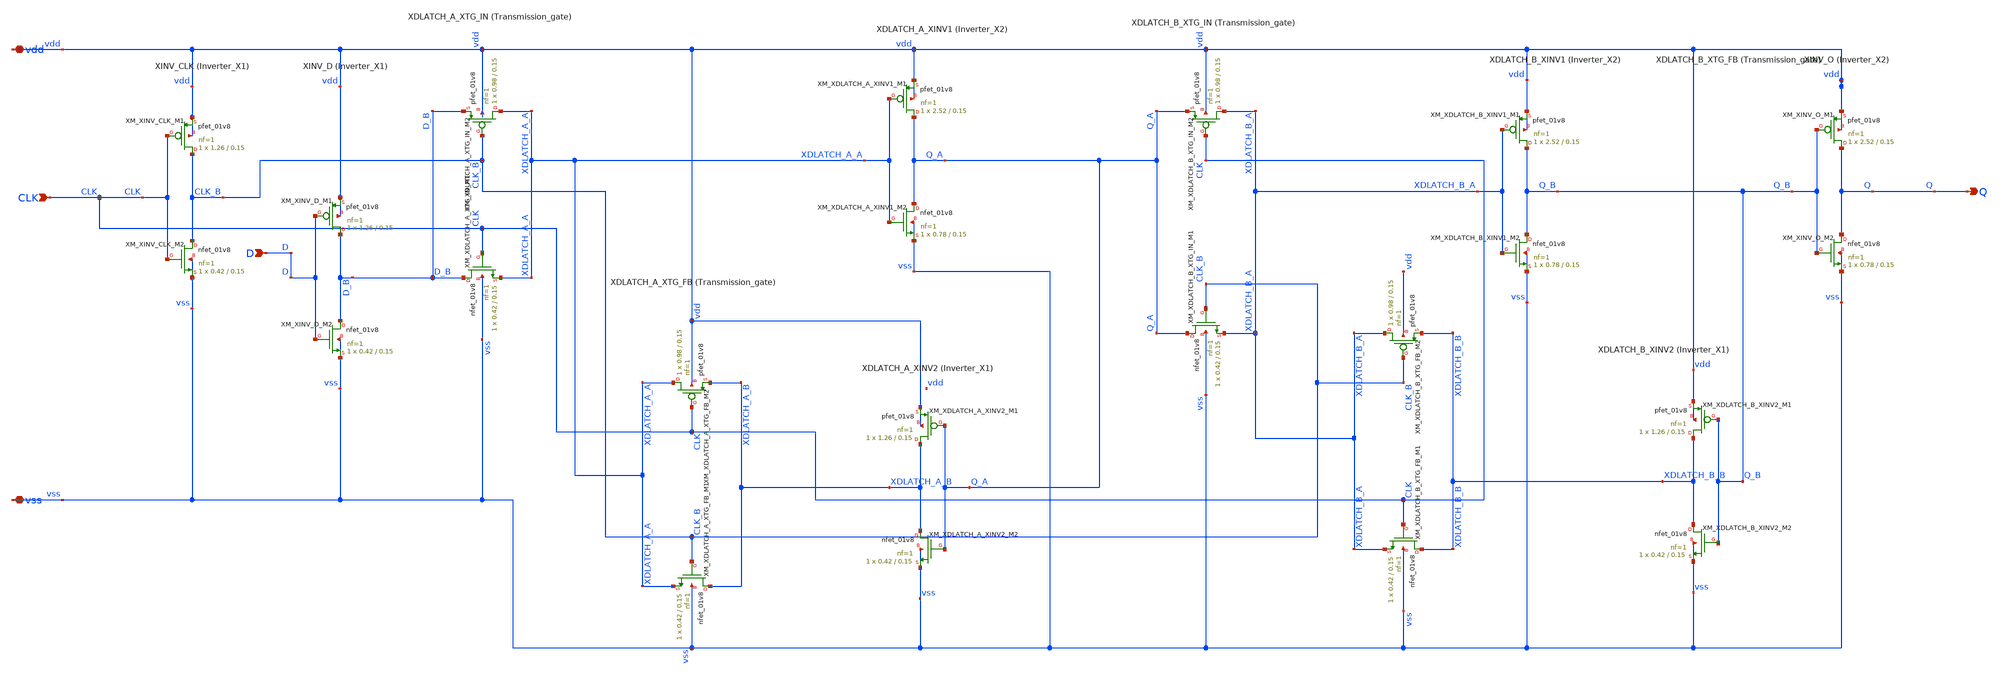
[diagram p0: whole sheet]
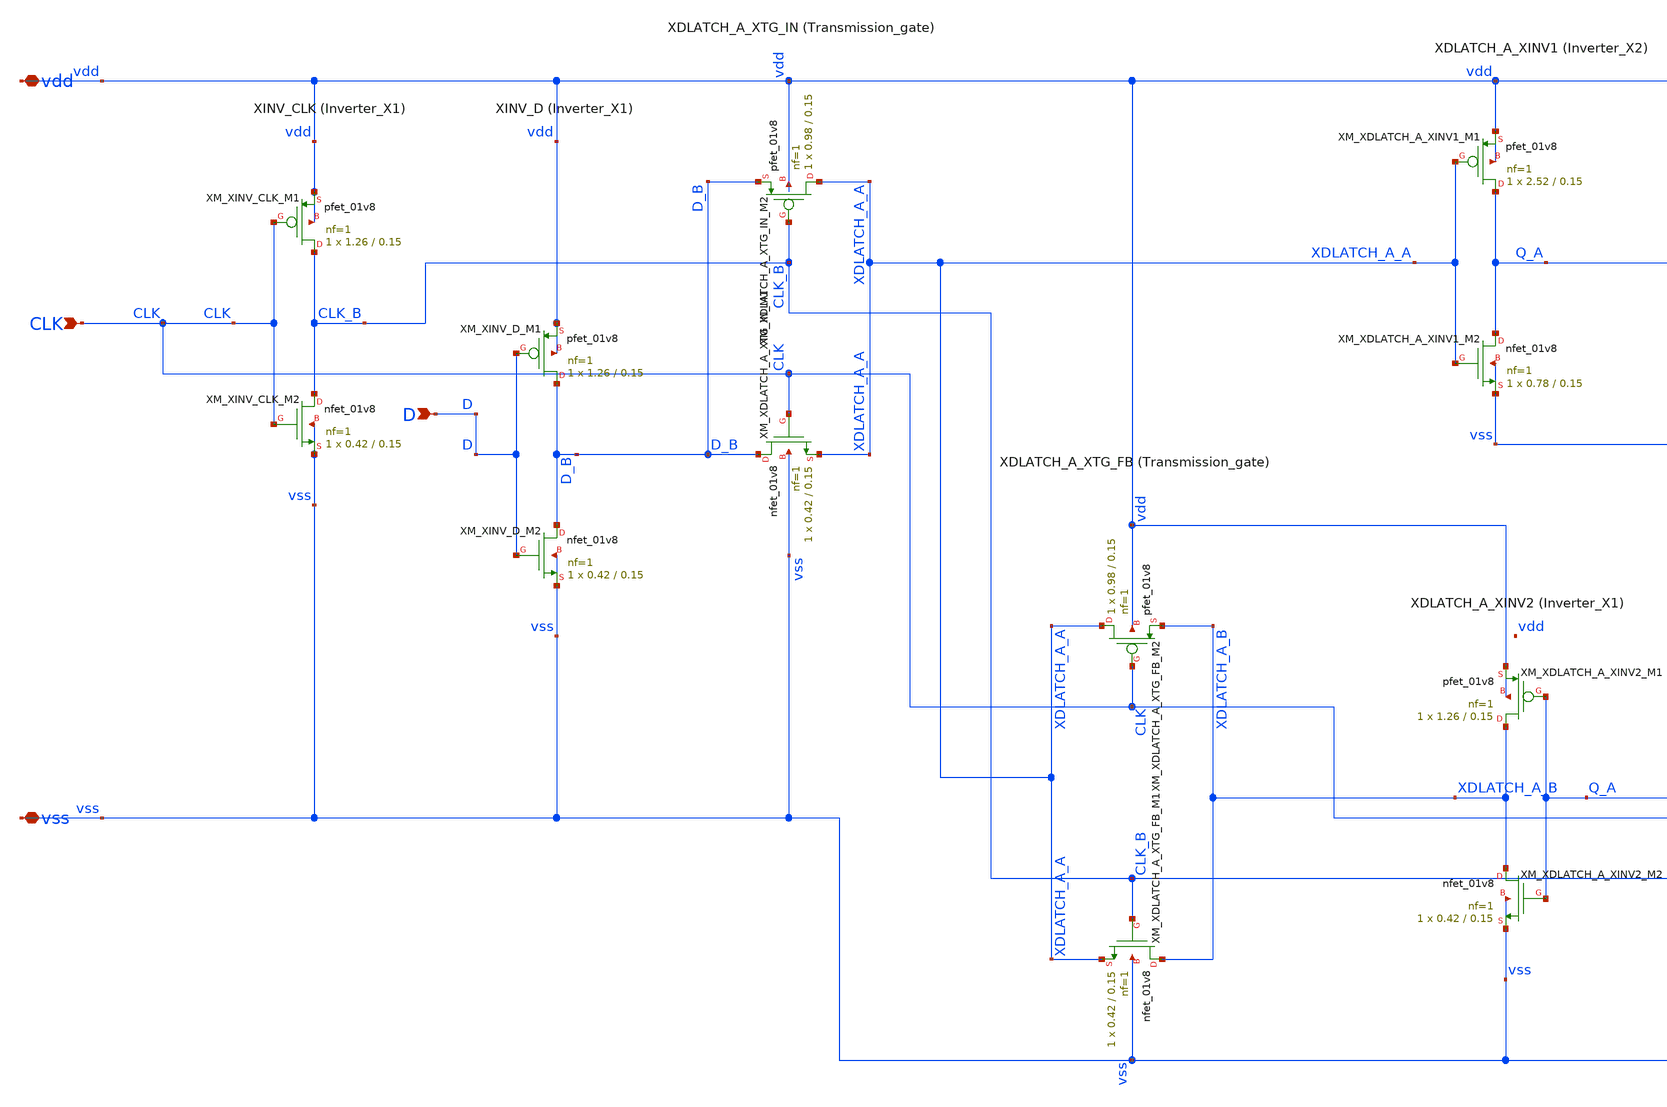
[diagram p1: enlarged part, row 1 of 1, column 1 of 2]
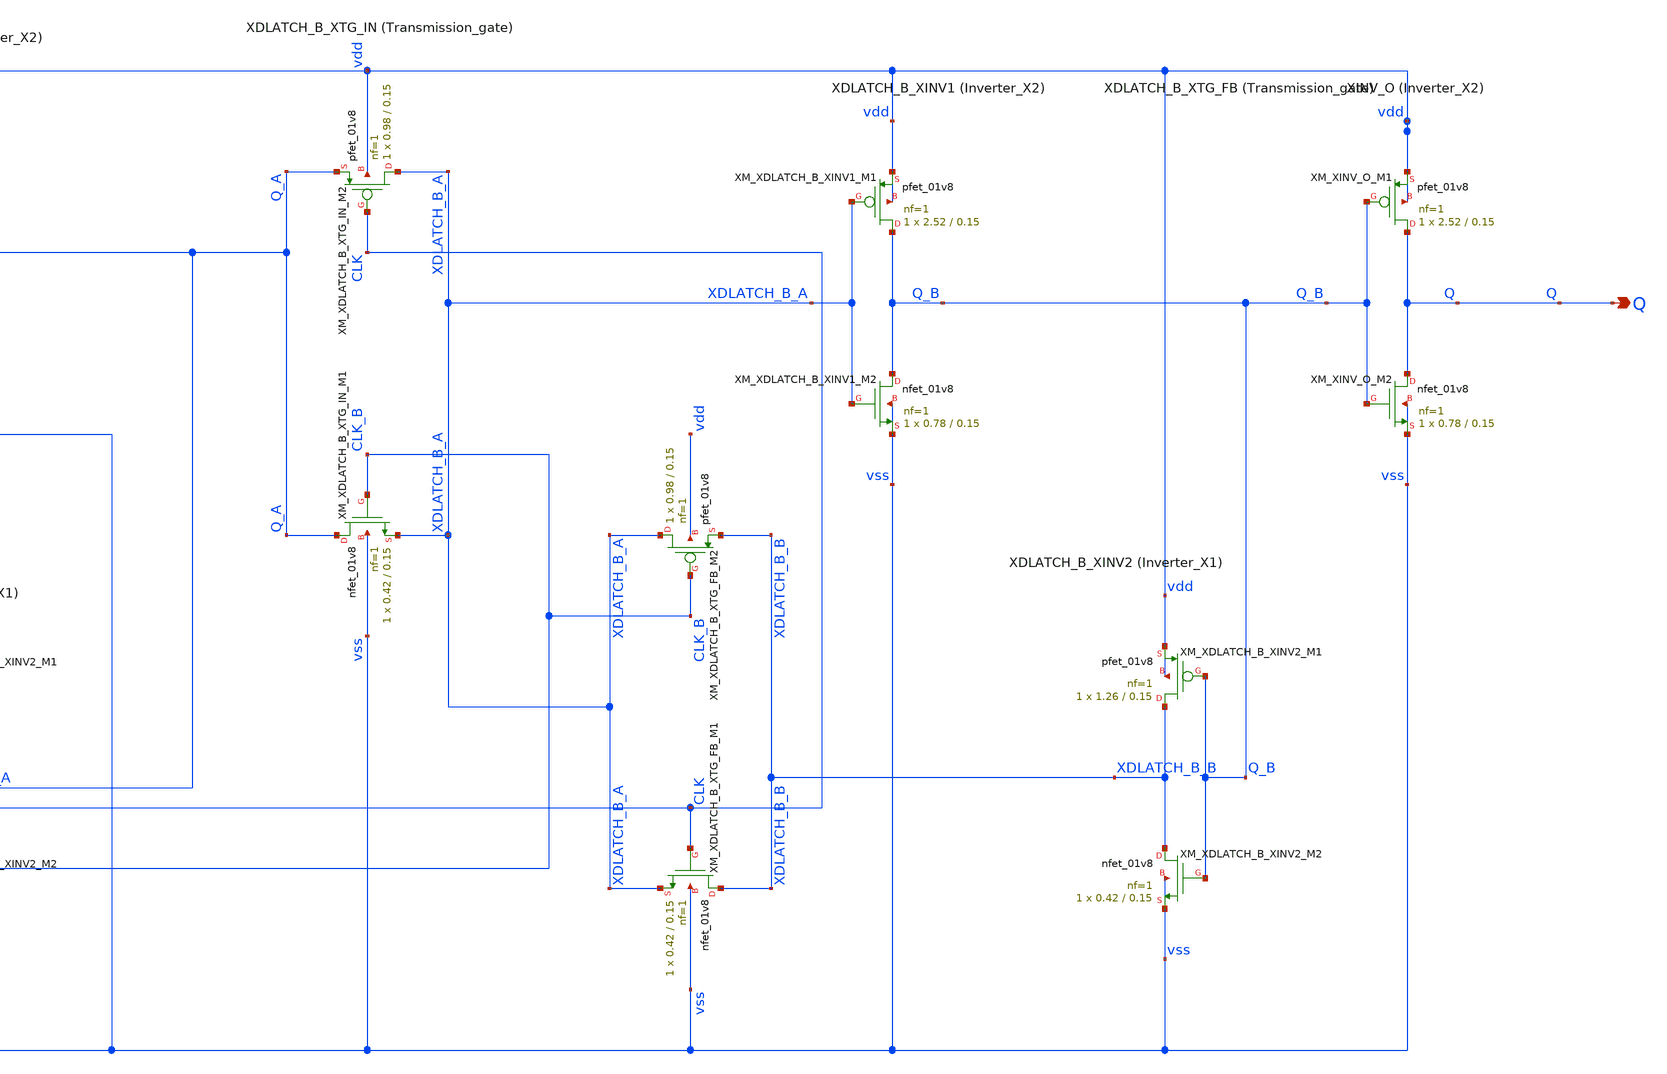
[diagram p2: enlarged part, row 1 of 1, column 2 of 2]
** sch_path: Spice_Netlist/Schematic/dfxtn_flat.sch
**.subckt dfxtn_flat vdd vss D CLK Q
*.iopin vdd
*.iopin vss
*.ipin D
*.ipin CLK
*.opin Q
XXM_XINV_CLK_M1 CLK_B CLK vdd vdd sky130_fd_pr__pfet_01v8 L=0.15 W=1.26 nf=1 ad='int((nf+1)/2) * W/nf * 0.29'
+ as='int((nf+2)/2) * W/nf * 0.29' pd='2*int((nf+1)/2) * (W/nf + 0.29)' ps='2*int((nf+2)/2) * (W/nf + 0.29)'
+ nrd='0.29 / W' nrs='0.29 / W' sa=0 sb=0 sd=0 mult=1 m=1
XXM_XINV_CLK_M2 CLK_B CLK vss vss sky130_fd_pr__nfet_01v8 L=0.15 W=0.42 nf=1 ad='int((1 + 1)/2) * 0.42 / 1 * 0.29'
+ as='int((1 + 2)/2) * 0.42 / 1 * 0.29' pd='2*int((1 + 1)/2) * (0.42 / 1 + 0.29)' ps='2*int((1 + 2)/2) * (0.42 / 1 + 0.29)'
+ nrd='0.29 / 0.42 ' nrs='0.29 / 0.42 ' sa=0 sb=0 sd=0 mult=1 m=1
XXM_XINV_D_M1 D_B D vdd vdd sky130_fd_pr__pfet_01v8 L=0.15 W=1.26 nf=1 ad='int((nf+1)/2) * W/nf * 0.29'
+ as='int((nf+2)/2) * W/nf * 0.29' pd='2*int((nf+1)/2) * (W/nf + 0.29)' ps='2*int((nf+2)/2) * (W/nf + 0.29)'
+ nrd='0.29 / W' nrs='0.29 / W' sa=0 sb=0 sd=0 mult=1 m=1
XXM_XINV_D_M2 D_B D vss vss sky130_fd_pr__nfet_01v8 L=0.15 W=0.42 nf=1 ad='int((1 + 1)/2) * 0.42 / 1 * 0.29'
+ as='int((1 + 2)/2) * 0.42 / 1 * 0.29' pd='2*int((1 + 1)/2) * (0.42 / 1 + 0.29)' ps='2*int((1 + 2)/2) * (0.42 / 1 + 0.29)'
+ nrd='0.29 / 0.42 ' nrs='0.29 / 0.42 ' sa=0 sb=0 sd=0 mult=1 m=1
XXM_XDLATCH_A_XTG_IN_M2 XDLATCH_A_A CLK_B D_B vdd sky130_fd_pr__pfet_01v8 L=0.15 W=0.98 nf=1 ad='int((nf+1)/2) * W/nf * 0.29'
+ as='int((nf+2)/2) * W/nf * 0.29' pd='2*int((nf+1)/2) * (W/nf + 0.29)' ps='2*int((nf+2)/2) * (W/nf + 0.29)'
+ nrd='0.29 / W' nrs='0.29 / W' sa=0 sb=0 sd=0 mult=1 m=1
XXM_XDLATCH_A_XTG_IN_M1 D_B CLK XDLATCH_A_A vss sky130_fd_pr__nfet_01v8 L=0.15 W=0.42 nf=1 ad='int((1 + 1)/2) * 0.42 / 1 * 0.29'
+ as='int((1 + 2)/2) * 0.42 / 1 * 0.29' pd='2*int((1 + 1)/2) * (0.42 / 1 + 0.29)' ps='2*int((1 + 2)/2) * (0.42 / 1 + 0.29)'
+ nrd='0.29 / 0.42 ' nrs='0.29 / 0.42 ' sa=0 sb=0 sd=0 mult=1 m=1
XXM_XDLATCH_A_XINV1_M1 Q_A XDLATCH_A_A vdd vdd sky130_fd_pr__pfet_01v8 L=0.15 W=2.52 nf=1 ad='int((nf+1)/2) * W/nf * 0.29'
+ as='int((nf+2)/2) * W/nf * 0.29' pd='2*int((nf+1)/2) * (W/nf + 0.29)' ps='2*int((nf+2)/2) * (W/nf + 0.29)'
+ nrd='0.29 / W' nrs='0.29 / W' sa=0 sb=0 sd=0 mult=1 m=1
XXM_XDLATCH_A_XINV1_M2 Q_A XDLATCH_A_A vss vss sky130_fd_pr__nfet_01v8 L=0.15 W=0.78 nf=1 ad='int((1 + 1)/2) * 0.78 / 1 * 0.29'
+ as='int((1 + 2)/2) * 0.78 / 1 * 0.29' pd='2*int((1 + 1)/2) * (0.78 / 1 + 0.29)' ps='2*int((1 + 2)/2) * (0.78 / 1 + 0.29)'
+ nrd='0.29 / 0.78 ' nrs='0.29 / 0.78 ' sa=0 sb=0 sd=0 mult=1 m=1
XXM_XDLATCH_A_XINV2_M1 XDLATCH_A_B Q_A vdd vdd sky130_fd_pr__pfet_01v8 L=0.15 W=1.26 nf=1 ad='int((nf+1)/2) * W/nf * 0.29'
+ as='int((nf+2)/2) * W/nf * 0.29' pd='2*int((nf+1)/2) * (W/nf + 0.29)' ps='2*int((nf+2)/2) * (W/nf + 0.29)'
+ nrd='0.29 / W' nrs='0.29 / W' sa=0 sb=0 sd=0 mult=1 m=1
XXM_XDLATCH_A_XINV2_M2 XDLATCH_A_B Q_A vss vss sky130_fd_pr__nfet_01v8 L=0.15 W=0.42 nf=1 ad='int((1 + 1)/2) * 0.42 / 1 * 0.29'
+ as='int((1 + 2)/2) * 0.42 / 1 * 0.29' pd='2*int((1 + 1)/2) * (0.42 / 1 + 0.29)' ps='2*int((1 + 2)/2) * (0.42 / 1 + 0.29)'
+ nrd='0.29 / 0.42 ' nrs='0.29 / 0.42 ' sa=0 sb=0 sd=0 mult=1 m=1
XXM_XDLATCH_A_XTG_FB_M2 XDLATCH_A_A CLK XDLATCH_A_B vdd sky130_fd_pr__pfet_01v8 L=0.15 W=0.98 nf=1 ad='int((nf+1)/2) * W/nf * 0.29'
+ as='int((nf+2)/2) * W/nf * 0.29' pd='2*int((nf+1)/2) * (W/nf + 0.29)' ps='2*int((nf+2)/2) * (W/nf + 0.29)'
+ nrd='0.29 / W' nrs='0.29 / W' sa=0 sb=0 sd=0 mult=1 m=1
XXM_XDLATCH_A_XTG_FB_M1 XDLATCH_A_B CLK_B XDLATCH_A_A vss sky130_fd_pr__nfet_01v8 L=0.15 W=0.42 nf=1
+ ad='int((1 + 1)/2) * 0.42 / 1 * 0.29' as='int((1 + 2)/2) * 0.42 / 1 * 0.29' pd='2*int((1 + 1)/2) * (0.42 / 1 + 0.29)'
+ ps='2*int((1 + 2)/2) * (0.42 / 1 + 0.29)' nrd='0.29 / 0.42 ' nrs='0.29 / 0.42 ' sa=0 sb=0 sd=0 mult=1
+ m=1
XXM_XDLATCH_B_XTG_IN_M2 XDLATCH_B_A CLK Q_A vdd sky130_fd_pr__pfet_01v8 L=0.15 W=0.98 nf=1 ad='int((nf+1)/2) * W/nf * 0.29'
+ as='int((nf+2)/2) * W/nf * 0.29' pd='2*int((nf+1)/2) * (W/nf + 0.29)' ps='2*int((nf+2)/2) * (W/nf + 0.29)'
+ nrd='0.29 / W' nrs='0.29 / W' sa=0 sb=0 sd=0 mult=1 m=1
XXM_XDLATCH_B_XTG_IN_M1 Q_A CLK_B XDLATCH_B_A vss sky130_fd_pr__nfet_01v8 L=0.15 W=0.42 nf=1 ad='int((1 + 1)/2) * 0.42 / 1 * 0.29'
+ as='int((1 + 2)/2) * 0.42 / 1 * 0.29' pd='2*int((1 + 1)/2) * (0.42 / 1 + 0.29)' ps='2*int((1 + 2)/2) * (0.42 / 1 + 0.29)'
+ nrd='0.29 / 0.42 ' nrs='0.29 / 0.42 ' sa=0 sb=0 sd=0 mult=1 m=1
XXM_XDLATCH_B_XINV1_M1 Q_B XDLATCH_B_A vdd vdd sky130_fd_pr__pfet_01v8 L=0.15 W=2.52 nf=1 ad='int((nf+1)/2) * W/nf * 0.29'
+ as='int((nf+2)/2) * W/nf * 0.29' pd='2*int((nf+1)/2) * (W/nf + 0.29)' ps='2*int((nf+2)/2) * (W/nf + 0.29)'
+ nrd='0.29 / W' nrs='0.29 / W' sa=0 sb=0 sd=0 mult=1 m=1
XXM_XDLATCH_B_XINV1_M2 Q_B XDLATCH_B_A vss vss sky130_fd_pr__nfet_01v8 L=0.15 W=0.78 nf=1 ad='int((1 + 1)/2) * 0.78 / 1 * 0.29'
+ as='int((1 + 2)/2) * 0.78 / 1 * 0.29' pd='2*int((1 + 1)/2) * (0.78 / 1 + 0.29)' ps='2*int((1 + 2)/2) * (0.78 / 1 + 0.29)'
+ nrd='0.29 / 0.78 ' nrs='0.29 / 0.78 ' sa=0 sb=0 sd=0 mult=1 m=1
XXM_XDLATCH_B_XINV2_M1 XDLATCH_B_B Q_B vdd vdd sky130_fd_pr__pfet_01v8 L=0.15 W=1.26 nf=1 ad='int((nf+1)/2) * W/nf * 0.29'
+ as='int((nf+2)/2) * W/nf * 0.29' pd='2*int((nf+1)/2) * (W/nf + 0.29)' ps='2*int((nf+2)/2) * (W/nf + 0.29)'
+ nrd='0.29 / W' nrs='0.29 / W' sa=0 sb=0 sd=0 mult=1 m=1
XXM_XDLATCH_B_XINV2_M2 XDLATCH_B_B Q_B vss vss sky130_fd_pr__nfet_01v8 L=0.15 W=0.42 nf=1 ad='int((1 + 1)/2) * 0.42 / 1 * 0.29'
+ as='int((1 + 2)/2) * 0.42 / 1 * 0.29' pd='2*int((1 + 1)/2) * (0.42 / 1 + 0.29)' ps='2*int((1 + 2)/2) * (0.42 / 1 + 0.29)'
+ nrd='0.29 / 0.42 ' nrs='0.29 / 0.42 ' sa=0 sb=0 sd=0 mult=1 m=1
XXM_XDLATCH_B_XTG_FB_M2 XDLATCH_B_A CLK_B XDLATCH_B_B vdd sky130_fd_pr__pfet_01v8 L=0.15 W=0.98 nf=1
+ ad='int((nf+1)/2) * W/nf * 0.29' as='int((nf+2)/2) * W/nf * 0.29' pd='2*int((nf+1)/2) * (W/nf + 0.29)'
+ ps='2*int((nf+2)/2) * (W/nf + 0.29)' nrd='0.29 / W' nrs='0.29 / W' sa=0 sb=0 sd=0 mult=1 m=1
XXM_XDLATCH_B_XTG_FB_M1 XDLATCH_B_B CLK XDLATCH_B_A vss sky130_fd_pr__nfet_01v8 L=0.15 W=0.42 nf=1 ad='int((1 + 1)/2) * 0.42 / 1 * 0.29'
+ as='int((1 + 2)/2) * 0.42 / 1 * 0.29' pd='2*int((1 + 1)/2) * (0.42 / 1 + 0.29)' ps='2*int((1 + 2)/2) * (0.42 / 1 + 0.29)'
+ nrd='0.29 / 0.42 ' nrs='0.29 / 0.42 ' sa=0 sb=0 sd=0 mult=1 m=1
XXM_XINV_O_M1 Q Q_B vdd vdd sky130_fd_pr__pfet_01v8 L=0.15 W=2.52 nf=1 ad='int((nf+1)/2) * W/nf * 0.29'
+ as='int((nf+2)/2) * W/nf * 0.29' pd='2*int((nf+1)/2) * (W/nf + 0.29)' ps='2*int((nf+2)/2) * (W/nf + 0.29)'
+ nrd='0.29 / W' nrs='0.29 / W' sa=0 sb=0 sd=0 mult=1 m=1
XXM_XINV_O_M2 Q Q_B vss vss sky130_fd_pr__nfet_01v8 L=0.15 W=0.78 nf=1 ad='int((1 + 1)/2) * 0.78 / 1 * 0.29'
+ as='int((1 + 2)/2) * 0.78 / 1 * 0.29' pd='2*int((1 + 1)/2) * (0.78 / 1 + 0.29)' ps='2*int((1 + 2)/2) * (0.78 / 1 + 0.29)'
+ nrd='0.29 / 0.78 ' nrs='0.29 / 0.78 ' sa=0 sb=0 sd=0 mult=1 m=1
**.ends
.end
